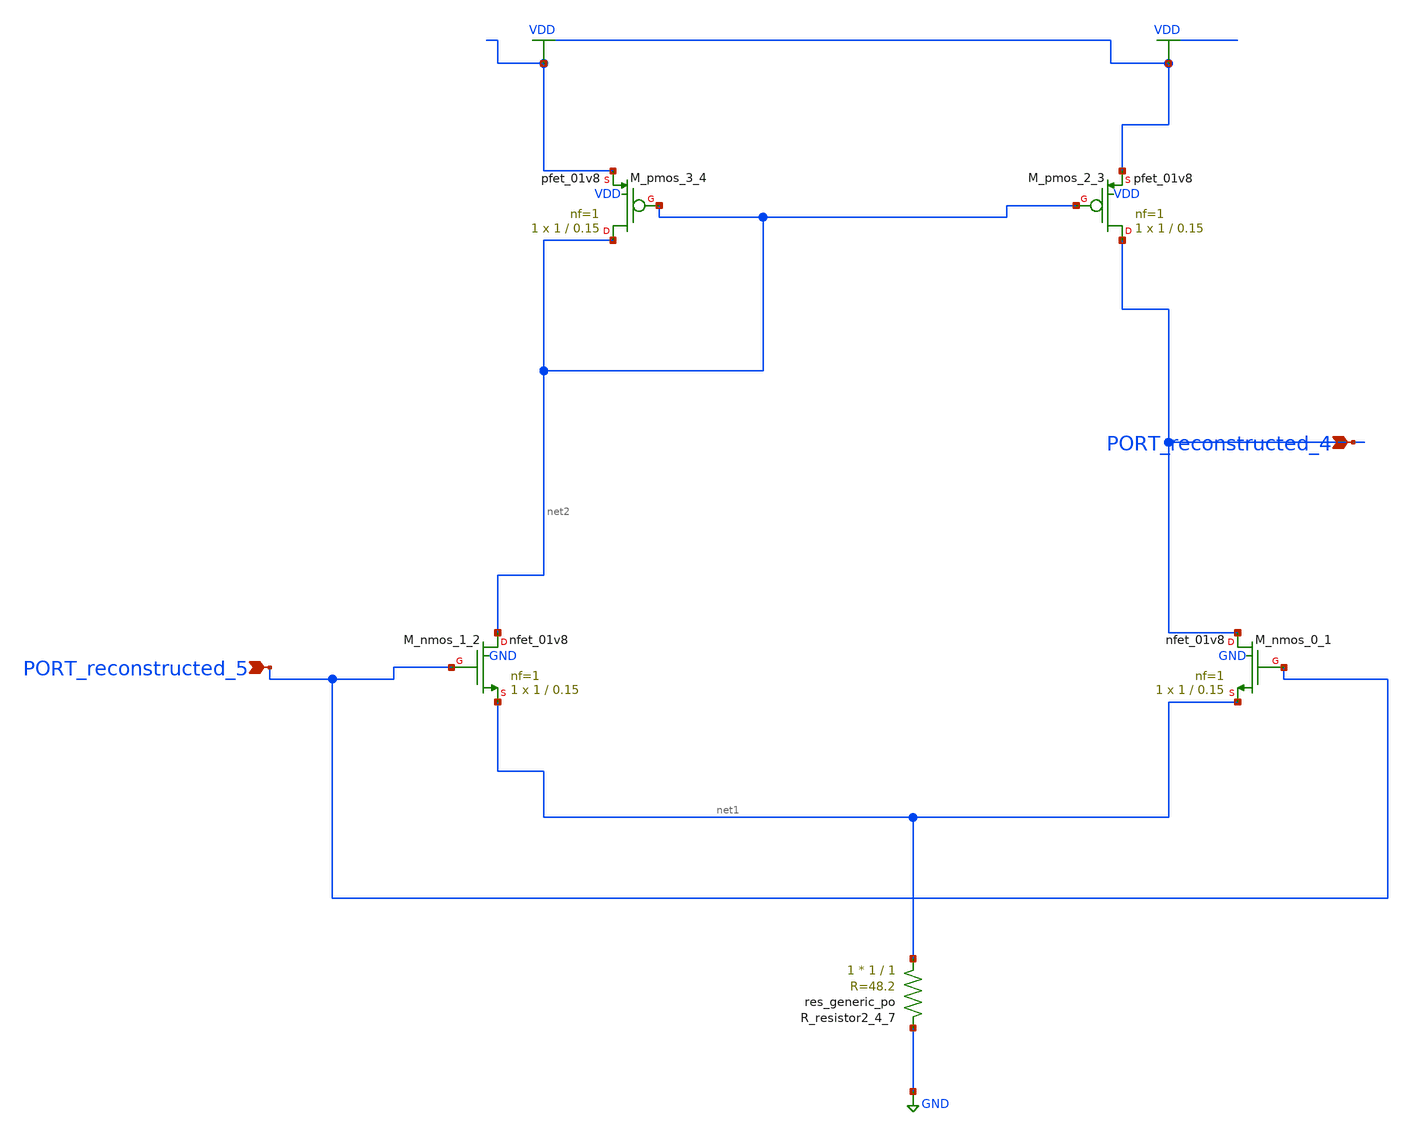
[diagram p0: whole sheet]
** sch_path: schematics/AMSNet/292.sch
**.subckt 292 PORT_reconstructed_4 PORT_reconstructed_5
*.ipin PORT_reconstructed_4
*.ipin PORT_reconstructed_5
XM_nmos_0_1 PORT_reconstructed_4 PORT_reconstructed_5 net1 GND sky130_fd_pr__nfet_01v8 L=0.15 W=1 nf=1
+ ad='int((1 + 1)/2) * 1 / 1 * 0.29' as='int((1 + 2)/2) * 1 / 1 * 0.29' pd='2*int((1 + 1)/2) * (1 / 1 + 0.29)'
+ ps='2*int((1 + 2)/2) * (1 / 1 + 0.29)' nrd='0.29 / 1 ' nrs='0.29 / 1 ' sa=0 sb=0 sd=0 mult=1 m=1
XM_nmos_1_2 net2 PORT_reconstructed_5 net1 GND sky130_fd_pr__nfet_01v8 L=0.15 W=1 nf=1 ad='int((1 + 1)/2) * 1 / 1 * 0.29'
+ as='int((1 + 2)/2) * 1 / 1 * 0.29' pd='2*int((1 + 1)/2) * (1 / 1 + 0.29)' ps='2*int((1 + 2)/2) * (1 / 1 + 0.29)'
+ nrd='0.29 / 1 ' nrs='0.29 / 1 ' sa=0 sb=0 sd=0 mult=1 m=1
XM_pmos_2_3 PORT_reconstructed_4 net2 VDD VDD sky130_fd_pr__pfet_01v8 L=0.15 W=1 nf=1 ad='int((1 + 1)/2) * 1 / 1 * 0.29'
+ as='int((1 + 2)/2) * 1 / 1 * 0.29' pd='2*int((1 + 1)/2) * (1 / 1 + 0.29)' ps='2*int((1 + 2)/2) * (1 / 1 + 0.29)'
+ nrd='0.29 / 1 ' nrs='0.29 / 1 ' sa=0 sb=0 sd=0 mult=1 m=1
XM_pmos_3_4 net2 net2 VDD VDD sky130_fd_pr__pfet_01v8 L=0.15 W=1 nf=1 ad='int((1 + 1)/2) * 1 / 1 * 0.29'
+ as='int((1 + 2)/2) * 1 / 1 * 0.29' pd='2*int((1 + 1)/2) * (1 / 1 + 0.29)' ps='2*int((1 + 2)/2) * (1 / 1 + 0.29)'
+ nrd='0.29 / 1 ' nrs='0.29 / 1 ' sa=0 sb=0 sd=0 mult=1 m=1
XR_resistor2_4_7 net1 GND sky130_fd_pr__res_generic_po W=1 L=1 m=1
**.ends
.GLOBAL GND
.GLOBAL VDD
.end
